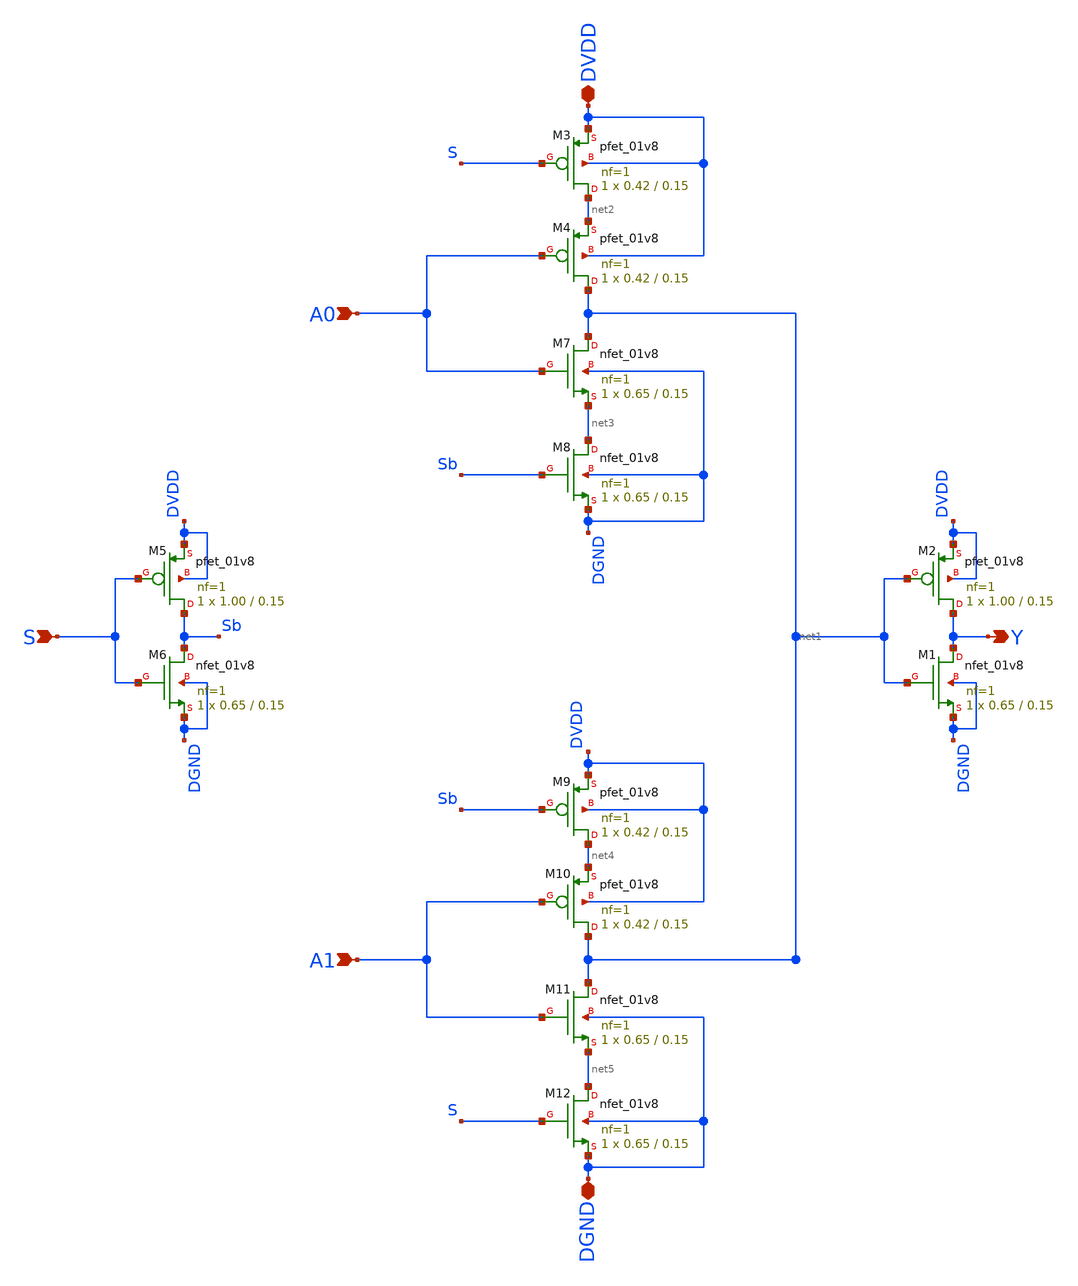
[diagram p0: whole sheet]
** sch_path: project/sch_sym_files/mux2.sch
**.subckt mux2 DVDD DGND A0 A1 S Y
*.iopin DVDD
*.iopin DGND
*.ipin A0
*.ipin A1
*.ipin S
*.opin Y
XM2 Y net1 DVDD DVDD sky130_fd_pr__pfet_01v8 L=0.15 W=1.00 nf=1 ad='int((nf+1)/2) * W/nf * 0.29' as='int((nf+2)/2) * W/nf * 0.29'
+ pd='2*int((nf+1)/2) * (W/nf + 0.29)' ps='2*int((nf+2)/2) * (W/nf + 0.29)' nrd='0.29 / W' nrs='0.29 / W'
+ sa=0 sb=0 sd=0 mult=1 m=1
XM1 Y net1 DGND DGND sky130_fd_pr__nfet_01v8 L=0.15 W=0.65 nf=1 ad='int((nf+1)/2) * W/nf * 0.29' as='int((nf+2)/2) * W/nf * 0.29'
+ pd='2*int((nf+1)/2) * (W/nf + 0.29)' ps='2*int((nf+2)/2) * (W/nf + 0.29)' nrd='0.29 / W' nrs='0.29 / W'
+ sa=0 sb=0 sd=0 mult=1 m=1
XM3 net2 S DVDD DVDD sky130_fd_pr__pfet_01v8 L=0.15 W=0.42 nf=1 ad='int((nf+1)/2) * W/nf * 0.29' as='int((nf+2)/2) * W/nf * 0.29'
+ pd='2*int((nf+1)/2) * (W/nf + 0.29)' ps='2*int((nf+2)/2) * (W/nf + 0.29)' nrd='0.29 / W' nrs='0.29 / W'
+ sa=0 sb=0 sd=0 mult=1 m=1
XM4 net1 A0 net2 DVDD sky130_fd_pr__pfet_01v8 L=0.15 W=0.42 nf=1 ad='int((nf+1)/2) * W/nf * 0.29' as='int((nf+2)/2) * W/nf * 0.29'
+ pd='2*int((nf+1)/2) * (W/nf + 0.29)' ps='2*int((nf+2)/2) * (W/nf + 0.29)' nrd='0.29 / W' nrs='0.29 / W'
+ sa=0 sb=0 sd=0 mult=1 m=1
XM5 Sb S DVDD DVDD sky130_fd_pr__pfet_01v8 L=0.15 W=1.00 nf=1 ad='int((nf+1)/2) * W/nf * 0.29' as='int((nf+2)/2) * W/nf * 0.29'
+ pd='2*int((nf+1)/2) * (W/nf + 0.29)' ps='2*int((nf+2)/2) * (W/nf + 0.29)' nrd='0.29 / W' nrs='0.29 / W'
+ sa=0 sb=0 sd=0 mult=1 m=1
XM6 Sb S DGND DGND sky130_fd_pr__nfet_01v8 L=0.15 W=0.65 nf=1 ad='int((nf+1)/2) * W/nf * 0.29' as='int((nf+2)/2) * W/nf * 0.29'
+ pd='2*int((nf+1)/2) * (W/nf + 0.29)' ps='2*int((nf+2)/2) * (W/nf + 0.29)' nrd='0.29 / W' nrs='0.29 / W'
+ sa=0 sb=0 sd=0 mult=1 m=1
XM7 net1 A0 net3 DGND sky130_fd_pr__nfet_01v8 L=0.15 W=0.65 nf=1 ad='int((nf+1)/2) * W/nf * 0.29' as='int((nf+2)/2) * W/nf * 0.29'
+ pd='2*int((nf+1)/2) * (W/nf + 0.29)' ps='2*int((nf+2)/2) * (W/nf + 0.29)' nrd='0.29 / W' nrs='0.29 / W'
+ sa=0 sb=0 sd=0 mult=1 m=1
XM8 net3 Sb DGND DGND sky130_fd_pr__nfet_01v8 L=0.15 W=0.65 nf=1 ad='int((nf+1)/2) * W/nf * 0.29' as='int((nf+2)/2) * W/nf * 0.29'
+ pd='2*int((nf+1)/2) * (W/nf + 0.29)' ps='2*int((nf+2)/2) * (W/nf + 0.29)' nrd='0.29 / W' nrs='0.29 / W'
+ sa=0 sb=0 sd=0 mult=1 m=1
XM9 net4 Sb DVDD DVDD sky130_fd_pr__pfet_01v8 L=0.15 W=0.42 nf=1 ad='int((nf+1)/2) * W/nf * 0.29' as='int((nf+2)/2) * W/nf * 0.29'
+ pd='2*int((nf+1)/2) * (W/nf + 0.29)' ps='2*int((nf+2)/2) * (W/nf + 0.29)' nrd='0.29 / W' nrs='0.29 / W'
+ sa=0 sb=0 sd=0 mult=1 m=1
XM10 net1 A1 net4 DVDD sky130_fd_pr__pfet_01v8 L=0.15 W=0.42 nf=1 ad='int((nf+1)/2) * W/nf * 0.29' as='int((nf+2)/2) * W/nf * 0.29'
+ pd='2*int((nf+1)/2) * (W/nf + 0.29)' ps='2*int((nf+2)/2) * (W/nf + 0.29)' nrd='0.29 / W' nrs='0.29 / W'
+ sa=0 sb=0 sd=0 mult=1 m=1
XM11 net1 A1 net5 DGND sky130_fd_pr__nfet_01v8 L=0.15 W=0.65 nf=1 ad='int((nf+1)/2) * W/nf * 0.29' as='int((nf+2)/2) * W/nf * 0.29'
+ pd='2*int((nf+1)/2) * (W/nf + 0.29)' ps='2*int((nf+2)/2) * (W/nf + 0.29)' nrd='0.29 / W' nrs='0.29 / W'
+ sa=0 sb=0 sd=0 mult=1 m=1
XM12 net5 S DGND DGND sky130_fd_pr__nfet_01v8 L=0.15 W=0.65 nf=1 ad='int((nf+1)/2) * W/nf * 0.29' as='int((nf+2)/2) * W/nf * 0.29'
+ pd='2*int((nf+1)/2) * (W/nf + 0.29)' ps='2*int((nf+2)/2) * (W/nf + 0.29)' nrd='0.29 / W' nrs='0.29 / W'
+ sa=0 sb=0 sd=0 mult=1 m=1
**.ends
.end
